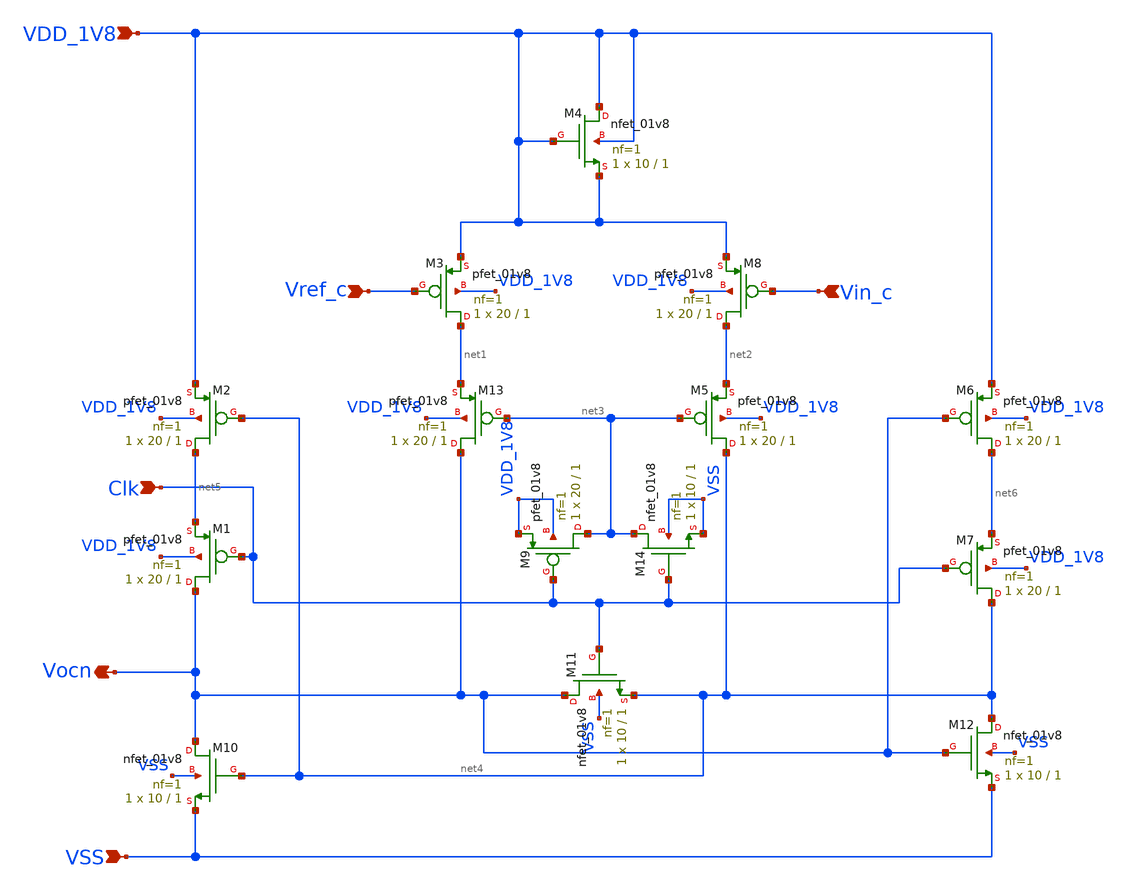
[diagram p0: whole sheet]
** sch_path: design/CNR_GR06_SKY130NM/comparator.sch
**.subckt comparator VDD_1V8 VSS Vin_c Vocn Clk Vref_c
*.ipin VDD_1V8
*.ipin VSS
*.ipin Vin_c
*.opin Vocn
*.ipin Clk
*.ipin Vref_c
XM1 Vocn Clk net5 VDD_1V8 sky130_fd_pr__pfet_01v8 L=1 W=20 nf=1 ad='int((nf+1)/2) * W/nf * 0.29' as='int((nf+2)/2) * W/nf * 0.29'
+ pd='2*int((nf+1)/2) * (W/nf + 0.29)' ps='2*int((nf+2)/2) * (W/nf + 0.29)' nrd='0.29 / W' nrs='0.29 / W'
+ sa=0 sb=0 sd=0 mult=1 m=1
XM2 net5 net4 VDD_1V8 VDD_1V8 sky130_fd_pr__pfet_01v8 L=1 W=20 nf=1 ad='int((nf+1)/2) * W/nf * 0.29'
+ as='int((nf+2)/2) * W/nf * 0.29' pd='2*int((nf+1)/2) * (W/nf + 0.29)' ps='2*int((nf+2)/2) * (W/nf + 0.29)'
+ nrd='0.29 / W' nrs='0.29 / W' sa=0 sb=0 sd=0 mult=1 m=1
XM3 net1 Vref_c VDD_1V8 VDD_1V8 sky130_fd_pr__pfet_01v8 L=1 W=20 nf=1 ad='int((nf+1)/2) * W/nf * 0.29'
+ as='int((nf+2)/2) * W/nf * 0.29' pd='2*int((nf+1)/2) * (W/nf + 0.29)' ps='2*int((nf+2)/2) * (W/nf + 0.29)'
+ nrd='0.29 / W' nrs='0.29 / W' sa=0 sb=0 sd=0 mult=1 m=1
XM5 net4 net3 net2 VDD_1V8 sky130_fd_pr__pfet_01v8 L=1 W=20 nf=1 ad='int((nf+1)/2) * W/nf * 0.29' as='int((nf+2)/2) * W/nf * 0.29'
+ pd='2*int((nf+1)/2) * (W/nf + 0.29)' ps='2*int((nf+2)/2) * (W/nf + 0.29)' nrd='0.29 / W' nrs='0.29 / W'
+ sa=0 sb=0 sd=0 mult=1 m=1
XM6 net6 Vocn VDD_1V8 VDD_1V8 sky130_fd_pr__pfet_01v8 L=1 W=20 nf=1 ad='int((nf+1)/2) * W/nf * 0.29'
+ as='int((nf+2)/2) * W/nf * 0.29' pd='2*int((nf+1)/2) * (W/nf + 0.29)' ps='2*int((nf+2)/2) * (W/nf + 0.29)'
+ nrd='0.29 / W' nrs='0.29 / W' sa=0 sb=0 sd=0 mult=1 m=1
XM7 net4 Clk net6 VDD_1V8 sky130_fd_pr__pfet_01v8 L=1 W=20 nf=1 ad='int((nf+1)/2) * W/nf * 0.29' as='int((nf+2)/2) * W/nf * 0.29'
+ pd='2*int((nf+1)/2) * (W/nf + 0.29)' ps='2*int((nf+2)/2) * (W/nf + 0.29)' nrd='0.29 / W' nrs='0.29 / W'
+ sa=0 sb=0 sd=0 mult=1 m=1
XM8 net2 Vin_c VDD_1V8 VDD_1V8 sky130_fd_pr__pfet_01v8 L=1 W=20 nf=1 ad='int((nf+1)/2) * W/nf * 0.29'
+ as='int((nf+2)/2) * W/nf * 0.29' pd='2*int((nf+1)/2) * (W/nf + 0.29)' ps='2*int((nf+2)/2) * (W/nf + 0.29)'
+ nrd='0.29 / W' nrs='0.29 / W' sa=0 sb=0 sd=0 mult=1 m=1
XM9 net3 Clk VDD_1V8 VDD_1V8 sky130_fd_pr__pfet_01v8 L=1 W=20 nf=1 ad='int((nf+1)/2) * W/nf * 0.29' as='int((nf+2)/2) * W/nf * 0.29'
+ pd='2*int((nf+1)/2) * (W/nf + 0.29)' ps='2*int((nf+2)/2) * (W/nf + 0.29)' nrd='0.29 / W' nrs='0.29 / W'
+ sa=0 sb=0 sd=0 mult=1 m=1
XM10 Vocn net4 VSS VSS sky130_fd_pr__nfet_01v8 L=1 W=10 nf=1 ad='int((nf+1)/2) * W/nf * 0.29' as='int((nf+2)/2) * W/nf * 0.29'
+ pd='2*int((nf+1)/2) * (W/nf + 0.29)' ps='2*int((nf+2)/2) * (W/nf + 0.29)' nrd='0.29 / W' nrs='0.29 / W'
+ sa=0 sb=0 sd=0 mult=1 m=1
XM11 Vocn Clk net4 VSS sky130_fd_pr__nfet_01v8 L=1 W=10 nf=1 ad='int((nf+1)/2) * W/nf * 0.29' as='int((nf+2)/2) * W/nf * 0.29'
+ pd='2*int((nf+1)/2) * (W/nf + 0.29)' ps='2*int((nf+2)/2) * (W/nf + 0.29)' nrd='0.29 / W' nrs='0.29 / W'
+ sa=0 sb=0 sd=0 mult=1 m=1
XM12 net4 Vocn VSS VSS sky130_fd_pr__nfet_01v8 L=1 W=10 nf=1 ad='int((nf+1)/2) * W/nf * 0.29' as='int((nf+2)/2) * W/nf * 0.29'
+ pd='2*int((nf+1)/2) * (W/nf + 0.29)' ps='2*int((nf+2)/2) * (W/nf + 0.29)' nrd='0.29 / W' nrs='0.29 / W'
+ sa=0 sb=0 sd=0 mult=1 m=1
XM13 Vocn net3 net1 VDD_1V8 sky130_fd_pr__pfet_01v8 L=1 W=20 nf=1 ad='int((nf+1)/2) * W/nf * 0.29' as='int((nf+2)/2) * W/nf * 0.29'
+ pd='2*int((nf+1)/2) * (W/nf + 0.29)' ps='2*int((nf+2)/2) * (W/nf + 0.29)' nrd='0.29 / W' nrs='0.29 / W'
+ sa=0 sb=0 sd=0 mult=1 m=1
XM14 net3 Clk VSS VSS sky130_fd_pr__nfet_01v8 L=1 W=10 nf=1 ad='int((nf+1)/2) * W/nf * 0.29' as='int((nf+2)/2) * W/nf * 0.29'
+ pd='2*int((nf+1)/2) * (W/nf + 0.29)' ps='2*int((nf+2)/2) * (W/nf + 0.29)' nrd='0.29 / W' nrs='0.29 / W'
+ sa=0 sb=0 sd=0 mult=1 m=1
XM4 VDD_1V8 VDD_1V8 VDD_1V8 VDD_1V8 sky130_fd_pr__nfet_01v8 L=1 W=10 nf=1 ad='int((nf+1)/2) * W/nf * 0.29'
+ as='int((nf+2)/2) * W/nf * 0.29' pd='2*int((nf+1)/2) * (W/nf + 0.29)' ps='2*int((nf+2)/2) * (W/nf + 0.29)'
+ nrd='0.29 / W' nrs='0.29 / W' sa=0 sb=0 sd=0 mult=1 m=1
**.ends
.end
